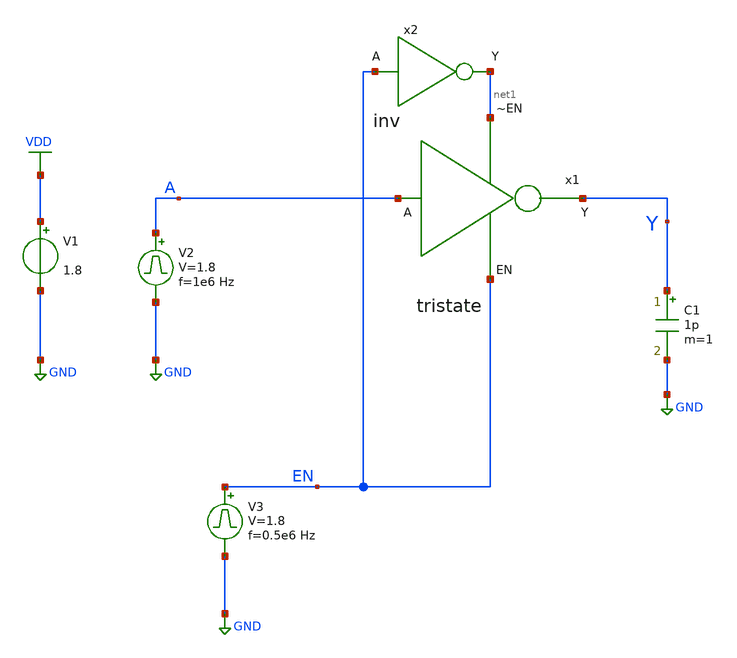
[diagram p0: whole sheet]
** sch_path: library/xschem/tristate_tb.sch
**.subckt tristate_tb
V1 VDD GND 1.8
V2 A GND pulse 0 1.8 '0.495/ 1e6 ' '0.01/1e6 ' '0.01/1e6 ' '0.49/1e6 ' '1/1e6 '
C1 Y GND 1p m=1
V3 EN GND pulse 0 1.8 '0.495/ 0.5e6 ' '0.01/0.5e6 ' '0.01/0.5e6 ' '0.49/0.5e6 ' '1/0.5e6 '
x1 net1 A Y EN tristate
x2 net1 EN inv
**** begin user architecture code


.control
save all
tran 1n 4u
plot V(A) V(EN)+2 V(Y)+4
.endc



** opencircuitdesign pdks install
.lib $::SKYWATER_MODELS/sky130.lib.spice tt


**** end user architecture code
**.ends

* expanding   symbol:  tristate.sym # of pins=4
** sym_path: library/xschem/tristate.sym
** sch_path: library/xschem/tristate.sch
.subckt tristate ~EN A Y EN
*.ipin A
*.opin Y
*.ipin EN
*.ipin ~EN
XM1 Y EN net1 GND sky130_fd_pr__nfet_01v8 L=0.15 W=0.5 nf=1 ad='int((nf+1)/2) * W/nf * 0.29' as='int((nf+2)/2) * W/nf * 0.29'
+ pd='2*int((nf+1)/2) * (W/nf + 0.29)' ps='2*int((nf+2)/2) * (W/nf + 0.29)' nrd='0.29 / W' nrs='0.29 / W'
+ sa=0 sb=0 sd=0 mult=1 m=1
XM2 Y ~EN net2 VDD sky130_fd_pr__pfet_01v8 L=0.15 W=1 nf=1 ad='int((nf+1)/2) * W/nf * 0.29' as='int((nf+2)/2) * W/nf * 0.29'
+ pd='2*int((nf+1)/2) * (W/nf + 0.29)' ps='2*int((nf+2)/2) * (W/nf + 0.29)' nrd='0.29 / W' nrs='0.29 / W'
+ sa=0 sb=0 sd=0 mult=1 m=1
XM3 net1 A GND GND sky130_fd_pr__nfet_01v8 L=0.15 W=0.5 nf=1 ad='int((nf+1)/2) * W/nf * 0.29' as='int((nf+2)/2) * W/nf * 0.29'
+ pd='2*int((nf+1)/2) * (W/nf + 0.29)' ps='2*int((nf+2)/2) * (W/nf + 0.29)' nrd='0.29 / W' nrs='0.29 / W'
+ sa=0 sb=0 sd=0 mult=1 m=1
XM4 net2 A VDD VDD sky130_fd_pr__pfet_01v8 L=0.15 W=1 nf=1 ad='int((nf+1)/2) * W/nf * 0.29' as='int((nf+2)/2) * W/nf * 0.29'
+ pd='2*int((nf+1)/2) * (W/nf + 0.29)' ps='2*int((nf+2)/2) * (W/nf + 0.29)' nrd='0.29 / W' nrs='0.29 / W'
+ sa=0 sb=0 sd=0 mult=1 m=1
.ends


* expanding   symbol:  lab1/inv.sym # of pins=2
** sym_path: library/xschem/lab1/inv.sym
** sch_path: library/xschem/lab1/inv.sch
.subckt inv Y A
*.ipin A
*.opin Y
XM1 Y A GND GND sky130_fd_pr__nfet_01v8 L=0.15 W=0.5 nf=1 ad='int((nf+1)/2) * W/nf * 0.29' as='int((nf+2)/2) * W/nf * 0.29'
+ pd='2*int((nf+1)/2) * (W/nf + 0.29)' ps='2*int((nf+2)/2) * (W/nf + 0.29)' nrd='0.29 / W' nrs='0.29 / W'
+ sa=0 sb=0 sd=0 mult=1 m=1
XM2 Y A VDD VDD sky130_fd_pr__pfet_01v8 L=0.15 W=1 nf=1 ad='int((nf+1)/2) * W/nf * 0.29' as='int((nf+2)/2) * W/nf * 0.29'
+ pd='2*int((nf+1)/2) * (W/nf + 0.29)' ps='2*int((nf+2)/2) * (W/nf + 0.29)' nrd='0.29 / W' nrs='0.29 / W'
+ sa=0 sb=0 sd=0 mult=1 m=1
.ends

.GLOBAL VDD
.GLOBAL GND
.end
